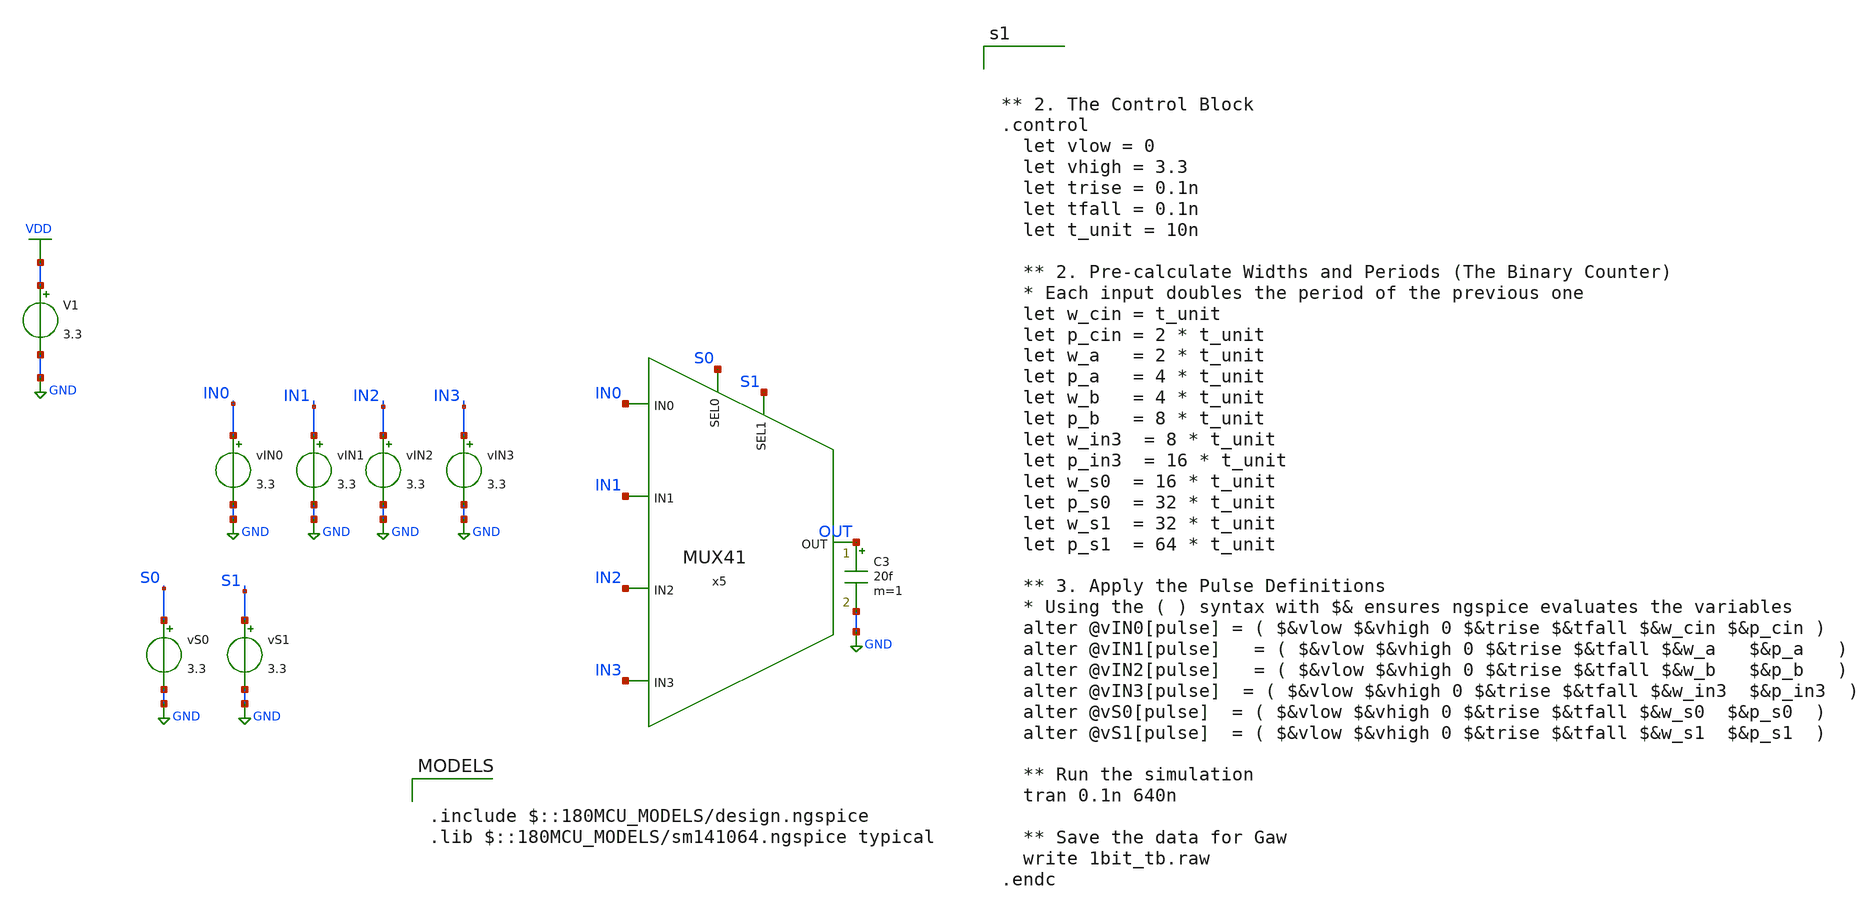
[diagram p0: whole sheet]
** sch_path: tbs/mux_tb.sch
**.subckt mux_tb
x5 S0 IN0 S1 IN1 OUT IN2 IN3 MUX41
vIN1 IN1 GND 3.3
vIN0 IN0 GND 3.3
vIN3 IN3 GND 3.3
vIN2 IN2 GND 3.3
vS1 S1 GND 3.3
vS0 S0 GND 3.3
C3 OUT GND 20f m=1
V1 VDD GND 3.3
**** begin user architecture code

.include $::180MCU_MODELS/design.ngspice
.lib $::180MCU_MODELS/sm141064.ngspice typical




** 2. The Control Block
.control
  let vlow = 0
  let vhigh = 3.3
  let trise = 0.1n
  let tfall = 0.1n
  let t_unit = 10n

  ** 2. Pre-calculate Widths and Periods (The Binary Counter)
  * Each input doubles the period of the previous one
  let w_cin = t_unit
  let p_cin = 2 * t_unit
  let w_a   = 2 * t_unit
  let p_a   = 4 * t_unit
  let w_b   = 4 * t_unit
  let p_b   = 8 * t_unit
  let w_in3  = 8 * t_unit
  let p_in3  = 16 * t_unit
  let w_s0  = 16 * t_unit
  let p_s0  = 32 * t_unit
  let w_s1  = 32 * t_unit
  let p_s1  = 64 * t_unit

  ** 3. Apply the Pulse Definitions
  * Using the ( ) syntax with $& ensures ngspice evaluates the variables
  alter @vIN0[pulse] = ( $&vlow $&vhigh 0 $&trise $&tfall $&w_cin $&p_cin )
  alter @vIN1[pulse]   = ( $&vlow $&vhigh 0 $&trise $&tfall $&w_a   $&p_a   )
  alter @vIN2[pulse]   = ( $&vlow $&vhigh 0 $&trise $&tfall $&w_b   $&p_b   )
  alter @vIN3[pulse]  = ( $&vlow $&vhigh 0 $&trise $&tfall $&w_in3  $&p_in3  )
  alter @vS0[pulse]  = ( $&vlow $&vhigh 0 $&trise $&tfall $&w_s0  $&p_s0  )
  alter @vS1[pulse]  = ( $&vlow $&vhigh 0 $&trise $&tfall $&w_s1  $&p_s1  )

  ** Run the simulation
  tran 0.1n 640n

  ** Save the data for Gaw
  write 1bit_tb.raw
.endc


**** end user architecture code
**.ends
.GLOBAL GND
.GLOBAL VDD
.end
